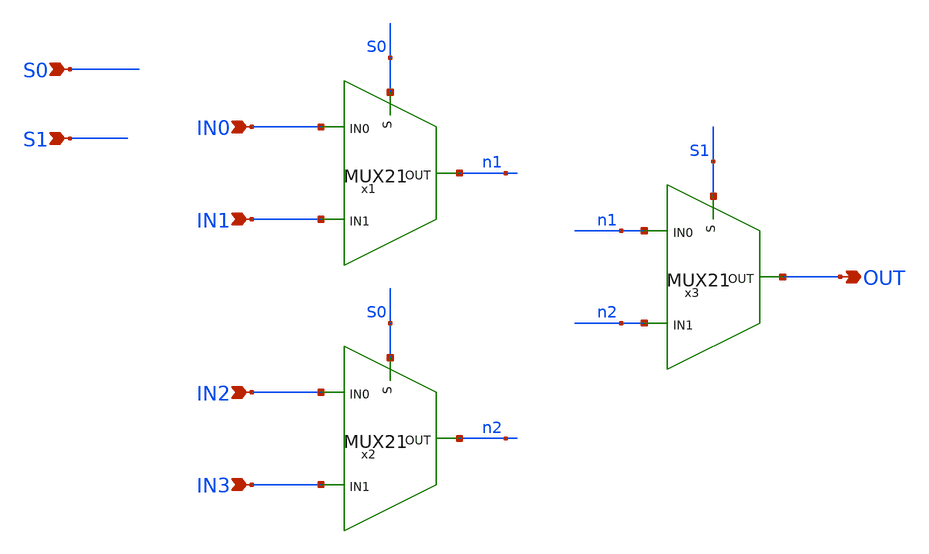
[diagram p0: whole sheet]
** sch_path: schematics/add/MUX41.sch
**.subckt MUX41 IN0 IN1 S0 S1 IN2 IN3 OUT
*.ipin IN0
*.ipin IN1
*.ipin S0
*.ipin S1
*.ipin IN2
*.ipin IN3
*.opin OUT
x1 IN0 S0 n1 IN1 MUX21
x2 IN2 S0 n2 IN3 MUX21
x3 n1 S1 OUT n2 MUX21
**.ends
.end
